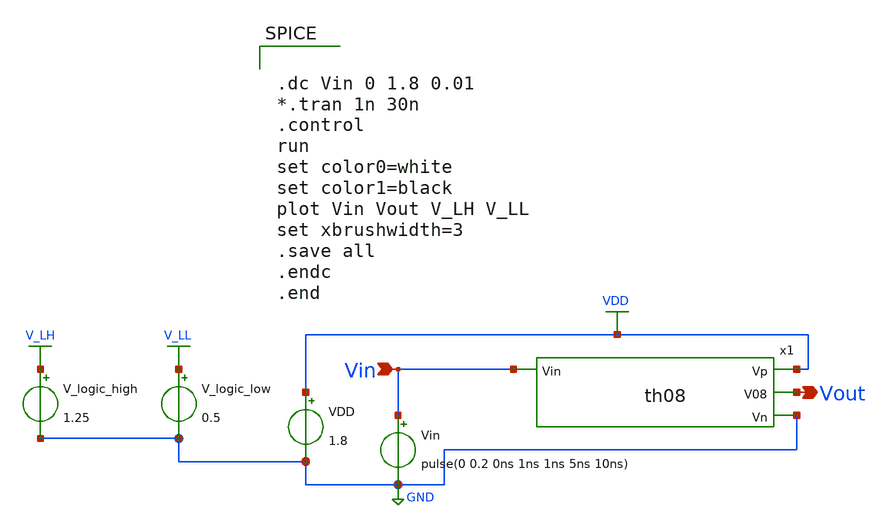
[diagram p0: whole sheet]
** sch_path: xschem/Vth_sch/Pre_layout/th08.sch
**.subckt th08 Vin Vout
*.ipin Vin
*.opin Vout
VDD VDD GND 1.8
Vin Vin GND pulse(0 0.2 0ns 1ns 1ns 5ns 10ns)
V_logic_high V_LH GND 1.25
V_logic_low V_LL GND 0.5
x1 VDD Vout Vin GND th08
**** begin user architecture code


.lib /usr/local/share/pdk/sky130A/libs.tech/ngspice/sky130.lib.spice tt

.save all





.dc Vin 0 1.8 0.01
*.tran 1n 30n
.control
run
set color0=white
set color1=black
plot Vin Vout V_LH V_LL
set xbrushwidth=3
.save all
.endc
.end


**** end user architecture code
**.ends

* expanding   symbol:  /home/exotic/Desktop/ASIC_ADC/xschem/Vth_sch/Symbol/th08.sym # of pins=4
** sym_path: xschem/Vth_sch/Symbol/th08.sym
** sch_path: xschem/Vth_sch/Symbol/th08.sch
.subckt th08 Vp V08 Vin Vn
*.opin Vn
*.opin Vp
*.ipin Vin
*.opin V08
XM2 V08 net1 Vp Vp sky130_fd_pr__pfet_01v8 L=0.48 W=0.43 nf=1 ad='int((nf+1)/2) * W/nf * 0.29' as='int((nf+2)/2) * W/nf * 0.29'
+ pd='2*int((nf+1)/2) * (W/nf + 0.29)' ps='2*int((nf+2)/2) * (W/nf + 0.29)' nrd='0.29 / W' nrs='0.29 / W'
+ sa=0 sb=0 sd=0 mult=1 m=1
XM3 V08 net1 Vn Vn sky130_fd_pr__nfet_01v8 L=0.15 W=0.468 nf=1 ad='int((nf+1)/2) * W/nf * 0.29' as='int((nf+2)/2) * W/nf * 0.29'
+ pd='2*int((nf+1)/2) * (W/nf + 0.29)' ps='2*int((nf+2)/2) * (W/nf + 0.29)' nrd='0.29 / W' nrs='0.29 / W'
+ sa=0 sb=0 sd=0 mult=1 m=1
XM1 net1 Vin Vp Vp sky130_fd_pr__pfet_01v8 L=0.16 W=0.668 nf=1 ad='int((nf+1)/2) * W/nf * 0.29' as='int((nf+2)/2) * W/nf * 0.29'
+ pd='2*int((nf+1)/2) * (W/nf + 0.29)' ps='2*int((nf+2)/2) * (W/nf + 0.29)' nrd='0.29 / W' nrs='0.29 / W'
+ sa=0 sb=0 sd=0 mult=1 m=1
XM0 net1 Vin Vn Vn sky130_fd_pr__nfet_01v8 L=1.13 W=0.36 nf=1 ad='int((nf+1)/2) * W/nf * 0.29' as='int((nf+2)/2) * W/nf * 0.29'
+ pd='2*int((nf+1)/2) * (W/nf + 0.29)' ps='2*int((nf+2)/2) * (W/nf + 0.29)' nrd='0.29 / W' nrs='0.29 / W'
+ sa=0 sb=0 sd=0 mult=1 m=1
.ends

.GLOBAL VDD
.GLOBAL GND
.GLOBAL V_LH
.GLOBAL V_LL
.end
